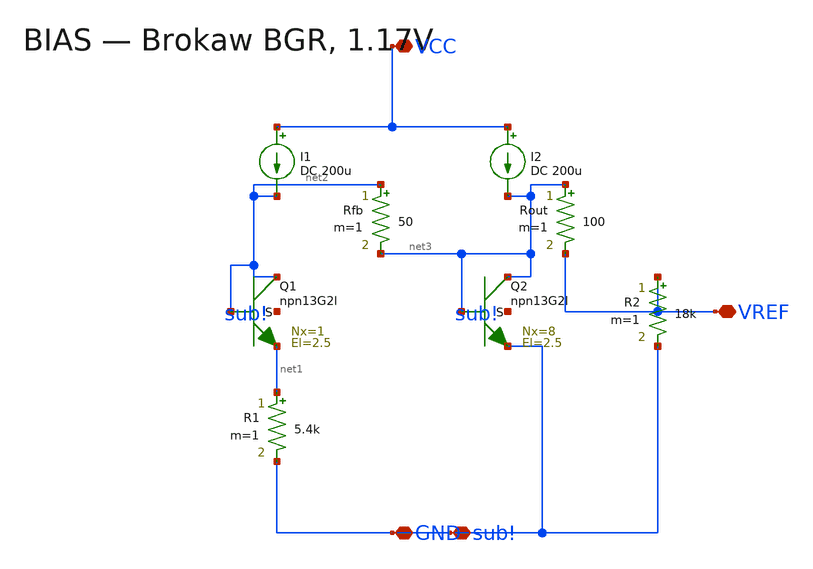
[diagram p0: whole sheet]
** sch_path: xschem/blocks/BIAS_BGR.sch
**.subckt BIAS_BGR VREF VCC GND sub!
*.iopin VREF
*.iopin VCC
*.iopin GND
*.iopin sub!
XQ1 net2 net2 net1 sub! npn13G2l Nx=1 El=2.5 mm_ok=1
XQ2 net3 net3 GND sub! npn13G2l Nx=8 El=2.5 mm_ok=1
R1 net1 GND 5.4k m=1
R2 VREF GND 18k m=1
Rfb net2 net3 50 m=1
Rout net3 VREF 100 m=1
I1 VCC net2 DC 200u
I2 VCC net3 DC 200u
**.ends
.end
